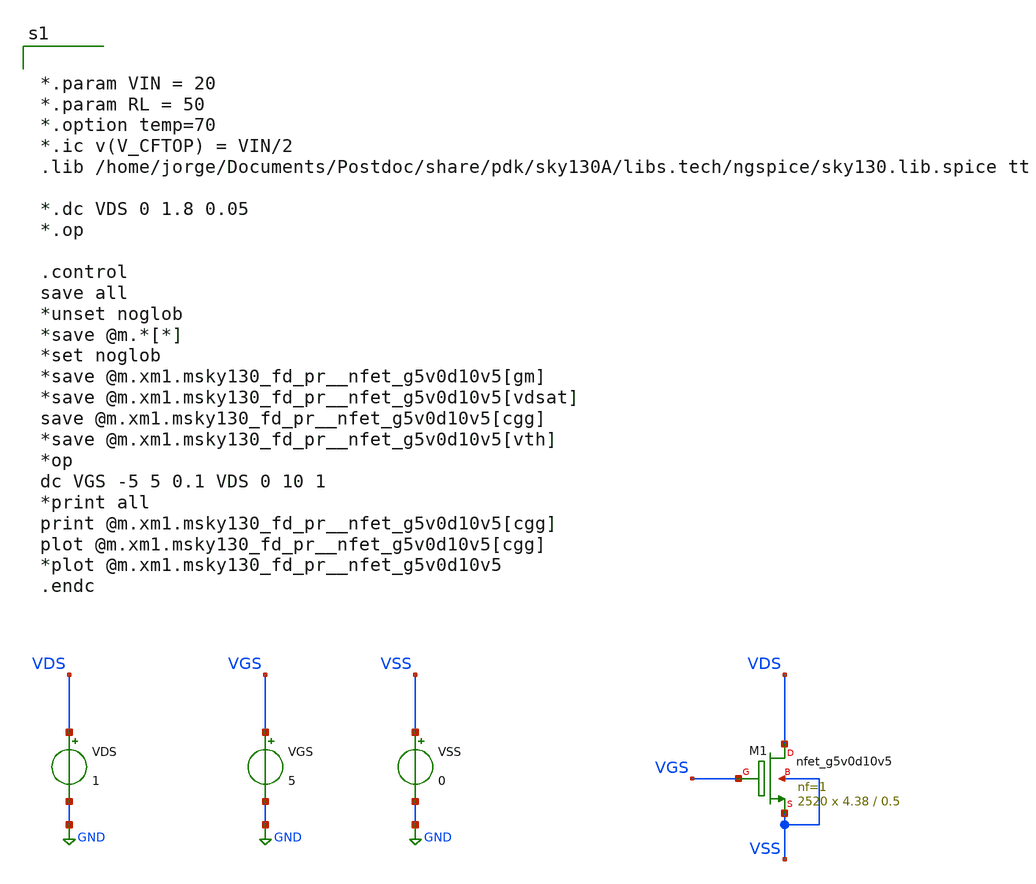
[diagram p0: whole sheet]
** sch_path: xschem/dev_switches/NMOSSW_full_OPsweep_v1p1_20220626.sch
**.subckt NMOSSW_full_OPsweep_v1p1_20220626
VGS VGS GND 5
VSS VSS GND 0
VDS VDS GND 1
XM1 VDS VGS VSS VSS sky130_fd_pr__nfet_g5v0d10v5 L=0.5 W=4.38 nf=1 ad='int((nf+1)/2) * W/nf * 0.29' as='int((nf+2)/2) * W/nf * 0.29'
+ pd='2*int((nf+1)/2) * (W/nf + 0.29)' ps='2*int((nf+2)/2) * (W/nf + 0.29)' nrd='0.29 / W' nrs='0.29 / W'
+ sa=0 sb=0 sd=0 mult=2520 m=2520
**** begin user architecture code


*.param VIN = 20
*.param RL = 50
*.option temp=70
*.ic v(V_CFTOP) = VIN/2
.lib /home/jorge/Documents/Postdoc/share/pdk/sky130A/libs.tech/ngspice/sky130.lib.spice tt

*.dc VDS 0 1.8 0.05
*.op

.control
save all
*unset noglob
*save @m.*[*]
*set noglob
*save @m.xm1.msky130_fd_pr__nfet_g5v0d10v5[gm]
*save @m.xm1.msky130_fd_pr__nfet_g5v0d10v5[vdsat]
save @m.xm1.msky130_fd_pr__nfet_g5v0d10v5[cgg]
*save @m.xm1.msky130_fd_pr__nfet_g5v0d10v5[vth]
*op
dc VGS -5 5 0.1 VDS 0 10 1
*print all
print @m.xm1.msky130_fd_pr__nfet_g5v0d10v5[cgg]
plot @m.xm1.msky130_fd_pr__nfet_g5v0d10v5[cgg]
*plot @m.xm1.msky130_fd_pr__nfet_g5v0d10v5
.endc



**** end user architecture code
**.ends
.GLOBAL GND
.end
